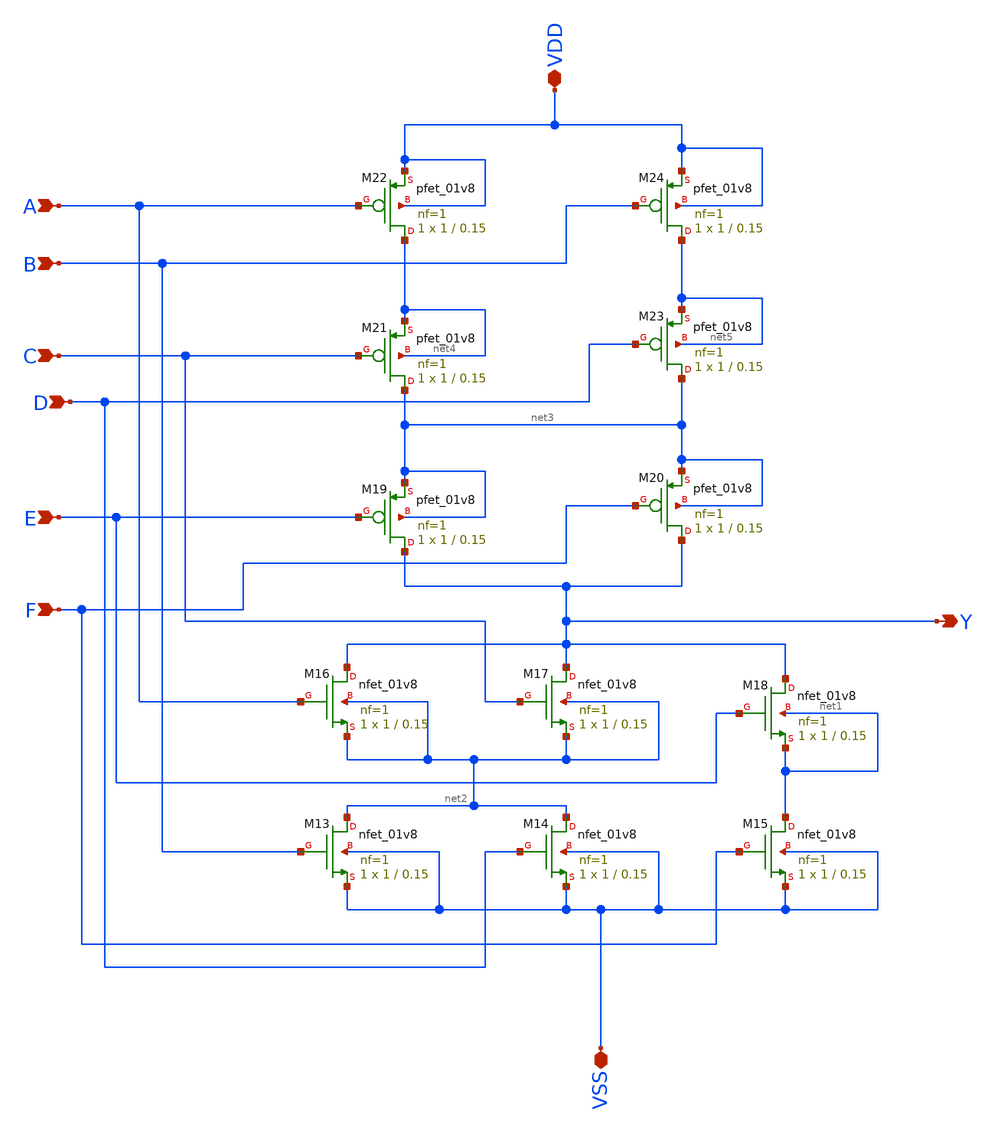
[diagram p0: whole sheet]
** sch_path: Week 1/xschem/test.sch
**.subckt test E F C D A B VDD VSS Y
*.ipin E
*.ipin F
*.ipin C
*.ipin D
*.ipin A
*.ipin B
*.iopin VDD
*.iopin VSS
*.opin Y
XM13 net2 B VSS VSS sky130_fd_pr__nfet_01v8 L=0.15 W=1 nf=1 ad='int((nf+1)/2) * W/nf * 0.29' as='int((nf+2)/2) * W/nf * 0.29'
+ pd='2*int((nf+1)/2) * (W/nf + 0.29)' ps='2*int((nf+2)/2) * (W/nf + 0.29)' nrd='0.29 / W' nrs='0.29 / W'
+ sa=0 sb=0 sd=0 mult=1 m=1
XM14 net2 D VSS VSS sky130_fd_pr__nfet_01v8 L=0.15 W=1 nf=1 ad='int((nf+1)/2) * W/nf * 0.29' as='int((nf+2)/2) * W/nf * 0.29'
+ pd='2*int((nf+1)/2) * (W/nf + 0.29)' ps='2*int((nf+2)/2) * (W/nf + 0.29)' nrd='0.29 / W' nrs='0.29 / W'
+ sa=0 sb=0 sd=0 mult=1 m=1
XM15 net1 F VSS VSS sky130_fd_pr__nfet_01v8 L=0.15 W=1 nf=1 ad='int((nf+1)/2) * W/nf * 0.29' as='int((nf+2)/2) * W/nf * 0.29'
+ pd='2*int((nf+1)/2) * (W/nf + 0.29)' ps='2*int((nf+2)/2) * (W/nf + 0.29)' nrd='0.29 / W' nrs='0.29 / W'
+ sa=0 sb=0 sd=0 mult=1 m=1
XM16 Y A net2 net2 sky130_fd_pr__nfet_01v8 L=0.15 W=1 nf=1 ad='int((nf+1)/2) * W/nf * 0.29' as='int((nf+2)/2) * W/nf * 0.29'
+ pd='2*int((nf+1)/2) * (W/nf + 0.29)' ps='2*int((nf+2)/2) * (W/nf + 0.29)' nrd='0.29 / W' nrs='0.29 / W'
+ sa=0 sb=0 sd=0 mult=1 m=1
XM17 Y C net2 net2 sky130_fd_pr__nfet_01v8 L=0.15 W=1 nf=1 ad='int((nf+1)/2) * W/nf * 0.29' as='int((nf+2)/2) * W/nf * 0.29'
+ pd='2*int((nf+1)/2) * (W/nf + 0.29)' ps='2*int((nf+2)/2) * (W/nf + 0.29)' nrd='0.29 / W' nrs='0.29 / W'
+ sa=0 sb=0 sd=0 mult=1 m=1
XM18 Y E net1 net1 sky130_fd_pr__nfet_01v8 L=0.15 W=1 nf=1 ad='int((nf+1)/2) * W/nf * 0.29' as='int((nf+2)/2) * W/nf * 0.29'
+ pd='2*int((nf+1)/2) * (W/nf + 0.29)' ps='2*int((nf+2)/2) * (W/nf + 0.29)' nrd='0.29 / W' nrs='0.29 / W'
+ sa=0 sb=0 sd=0 mult=1 m=1
XM19 Y E net3 net3 sky130_fd_pr__pfet_01v8 L=0.15 W=1 nf=1 ad='int((nf+1)/2) * W/nf * 0.29' as='int((nf+2)/2) * W/nf * 0.29'
+ pd='2*int((nf+1)/2) * (W/nf + 0.29)' ps='2*int((nf+2)/2) * (W/nf + 0.29)' nrd='0.29 / W' nrs='0.29 / W'
+ sa=0 sb=0 sd=0 mult=1 m=1
XM20 Y F net3 net3 sky130_fd_pr__pfet_01v8 L=0.15 W=1 nf=1 ad='int((nf+1)/2) * W/nf * 0.29' as='int((nf+2)/2) * W/nf * 0.29'
+ pd='2*int((nf+1)/2) * (W/nf + 0.29)' ps='2*int((nf+2)/2) * (W/nf + 0.29)' nrd='0.29 / W' nrs='0.29 / W'
+ sa=0 sb=0 sd=0 mult=1 m=1
XM21 net3 C net4 net4 sky130_fd_pr__pfet_01v8 L=0.15 W=1 nf=1 ad='int((nf+1)/2) * W/nf * 0.29' as='int((nf+2)/2) * W/nf * 0.29'
+ pd='2*int((nf+1)/2) * (W/nf + 0.29)' ps='2*int((nf+2)/2) * (W/nf + 0.29)' nrd='0.29 / W' nrs='0.29 / W'
+ sa=0 sb=0 sd=0 mult=1 m=1
XM22 net4 A VDD VDD sky130_fd_pr__pfet_01v8 L=0.15 W=1 nf=1 ad='int((nf+1)/2) * W/nf * 0.29' as='int((nf+2)/2) * W/nf * 0.29'
+ pd='2*int((nf+1)/2) * (W/nf + 0.29)' ps='2*int((nf+2)/2) * (W/nf + 0.29)' nrd='0.29 / W' nrs='0.29 / W'
+ sa=0 sb=0 sd=0 mult=1 m=1
XM23 net3 D net5 net5 sky130_fd_pr__pfet_01v8 L=0.15 W=1 nf=1 ad='int((nf+1)/2) * W/nf * 0.29' as='int((nf+2)/2) * W/nf * 0.29'
+ pd='2*int((nf+1)/2) * (W/nf + 0.29)' ps='2*int((nf+2)/2) * (W/nf + 0.29)' nrd='0.29 / W' nrs='0.29 / W'
+ sa=0 sb=0 sd=0 mult=1 m=1
XM24 net5 B VDD VDD sky130_fd_pr__pfet_01v8 L=0.15 W=1 nf=1 ad='int((nf+1)/2) * W/nf * 0.29' as='int((nf+2)/2) * W/nf * 0.29'
+ pd='2*int((nf+1)/2) * (W/nf + 0.29)' ps='2*int((nf+2)/2) * (W/nf + 0.29)' nrd='0.29 / W' nrs='0.29 / W'
+ sa=0 sb=0 sd=0 mult=1 m=1
**.ends
.end
